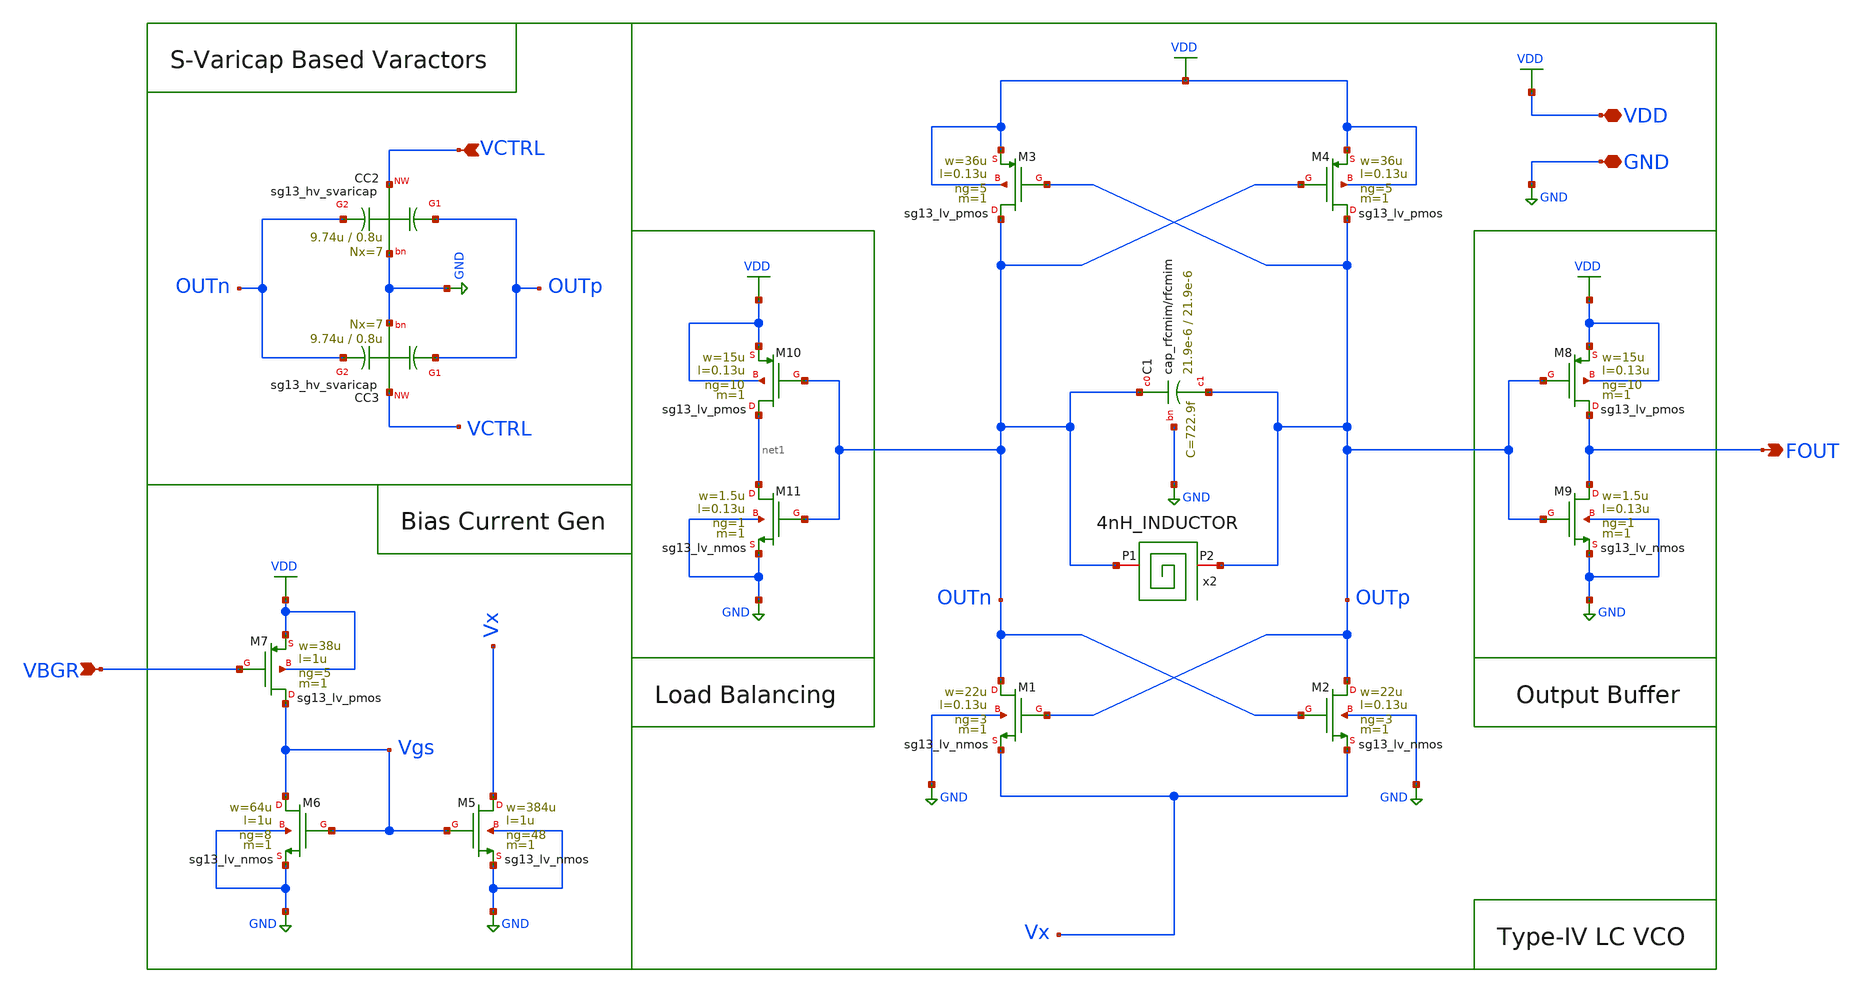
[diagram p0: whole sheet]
** sch_path: xschem/lc-vco/LC_VCO.sch
**.subckt LC_VCO FOUT VCTRL VBGR VDD GND
*.opin FOUT
*.ipin VCTRL
*.ipin VBGR
*.iopin VDD
*.iopin GND
XM5 Vx Vgs GND GND sg13_lv_nmos w=384u l=1u ng=48 m=1 mm_ok=1
XM4 OUTp OUTn VDD VDD sg13_lv_pmos w=36u l=0.13u ng=5 m=1 mm_ok=1
XM3 OUTn OUTp VDD VDD sg13_lv_pmos w=36u l=0.13u ng=5 m=1 mm_ok=1
XM2 OUTp OUTn Vx GND sg13_lv_nmos w=22u l=0.13u ng=3 m=1 mm_ok=1
XM1 OUTn OUTp Vx GND sg13_lv_nmos w=22u l=0.13u ng=3 m=1 mm_ok=1
XM6 Vgs Vgs GND GND sg13_lv_nmos w=64u l=1u ng=8 m=1 mm_ok=1
XC1 OUTn OUTp GND cap_rfcmim w=21.9e-6 l=21.9e-6 wfeed=10.0e-6 m=1 mm_ok=1
XC3 OUTp VCTRL OUTn GND sg13_hv_svaricap w=9.74u l=0.8u Nx=7
XC2 OUTp VCTRL OUTn GND sg13_hv_svaricap w=9.74u l=0.8u Nx=7
XM7 Vgs VBGR VDD VDD sg13_lv_pmos w=38u l=1u ng=5 m=1 mm_ok=1
XM8 FOUT OUTp VDD VDD sg13_lv_pmos w=15u l=0.13u ng=10 m=1 mm_ok=1
XM9 FOUT OUTp GND GND sg13_lv_nmos w=1.5u l=0.13u ng=1 m=1 mm_ok=1
XM10 net1 OUTn VDD VDD sg13_lv_pmos w=15u l=0.13u ng=10 m=1 mm_ok=1
XM11 net1 OUTn GND GND sg13_lv_nmos w=1.5u l=0.13u ng=1 m=1 mm_ok=1
x2 OUTn OUTp 4nH_INDUCTOR
**** begin user architecture code


.subckt 4nH_INDUCTOR 1 2
* LVS black-box stub only
* Full model is available in 4nH_INDUCTOR.spice
.ends


**** end user architecture code
**.ends
.GLOBAL GND
.GLOBAL VDD
.end
